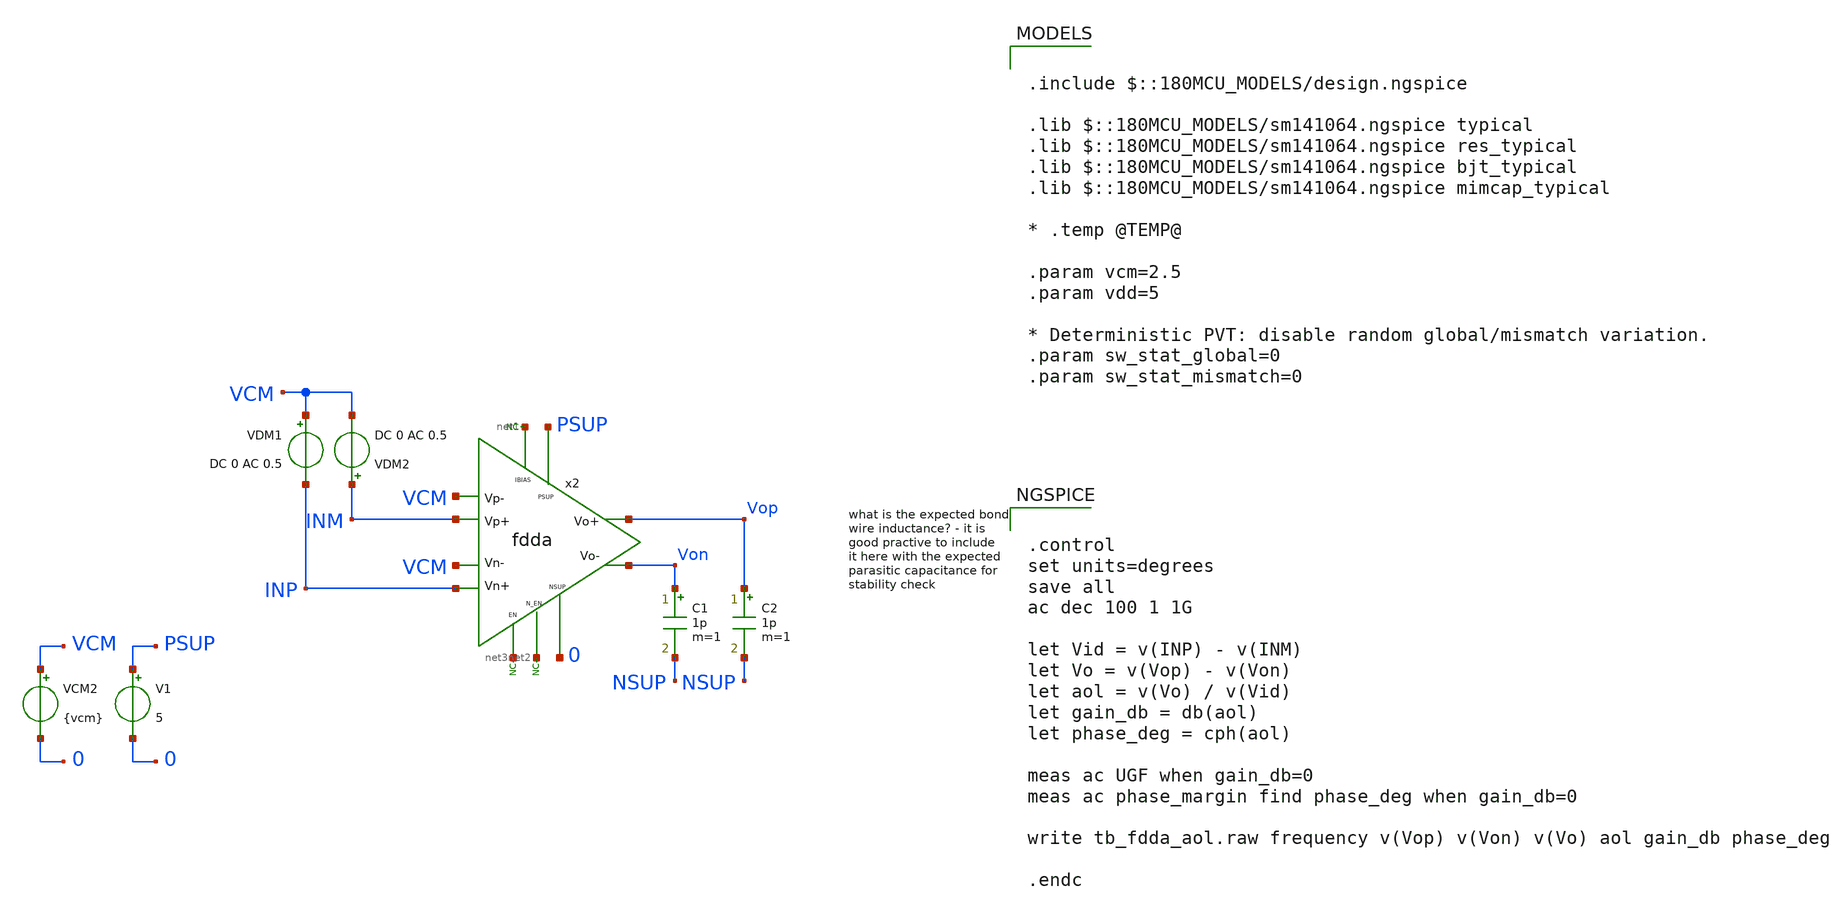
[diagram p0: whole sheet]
** sch_path: xschem/blocks/fdda/tb_fdda_aol.sch
**.subckt tb_fdda_aol
C1 Von NSUP 1p m=1
x2 PSUP VCM VCM INP INM Vop Von net1 net2 net3 0 fdda
* noconn #net1
* noconn #net3
* noconn #net2
V1 PSUP 0 5
C2 Vop NSUP 1p m=1
VCM2 VCM 0 {vcm}
VDM2 INM VCM DC 0 AC 0.5
VDM1 VCM INP DC 0 AC 0.5
**** begin user architecture code

.include $::180MCU_MODELS/design.ngspice

.lib $::180MCU_MODELS/sm141064.ngspice typical
.lib $::180MCU_MODELS/sm141064.ngspice res_typical
.lib $::180MCU_MODELS/sm141064.ngspice bjt_typical
.lib $::180MCU_MODELS/sm141064.ngspice mimcap_typical

* .temp @TEMP@

.param vcm=2.5
.param vdd=5

* Deterministic PVT: disable random global/mismatch variation.
.param sw_stat_global=0
.param sw_stat_mismatch=0



.control
set units=degrees
save all
ac dec 100 1 1G

let Vid = v(INP) - v(INM)
let Vo = v(Vop) - v(Von)
let aol = v(Vo) / v(Vid)
let gain_db = db(aol)
let phase_deg = cph(aol)

meas ac UGF when gain_db=0
meas ac phase_margin find phase_deg when gain_db=0

write tb_fdda_aol.raw frequency v(Vop) v(Von) v(Vo) aol gain_db phase_deg

.endc


**** end user architecture code
**.ends

* expanding   symbol:  blocks/fdda/fdda.sym # of pins=11
** sym_path: xschem/blocks/fdda/fdda.sym
** sch_path: xschem/blocks/fdda/fdda.sch
.subckt fdda PSUP Vp- Vn+ Vn- Vp+ Vo+ Vo- IBIAS N_EN EN NSUP
*.ipin PSUP
*.ipin NSUP
*.ipin N_EN
*.ipin EN
*.ipin IBIAS
*.ipin Vp+
*.ipin Vp-
*.ipin Vn+
*.ipin Vn-
*.opin Vo+
*.opin Vo-
* noconn N_EN
* noconn EN
I0 net5 NSUP 1u
XM9 Vo+ Vp- net1 NSUP pfet_06v0 L=2u W=4u nf=5 ad='int((nf+1)/2) * W/nf * 0.18u' as='int((nf+2)/2) * W/nf * 0.18u'
+ pd='2*int((nf+1)/2) * (W/nf + 0.18u)' ps='2*int((nf+2)/2) * (W/nf + 0.18u)' nrd='0.18u / W' nrs='0.18u / W'
+ sa=0 sb=0 sd=0 m=10
XM1 Vo- Vp+ net1 NSUP pfet_06v0 L=2u W=4u nf=5 ad='int((nf+1)/2) * W/nf * 0.18u' as='int((nf+2)/2) * W/nf * 0.18u'
+ pd='2*int((nf+1)/2) * (W/nf + 0.18u)' ps='2*int((nf+2)/2) * (W/nf + 0.18u)' nrd='0.18u / W' nrs='0.18u / W'
+ sa=0 sb=0 sd=0 m=10
XM2 net1 vb1 PSUP net3 pfet_06v0 L=4u W=2u nf=1 ad='int((nf+1)/2) * W/nf * 0.18u' as='int((nf+2)/2) * W/nf * 0.18u'
+ pd='2*int((nf+1)/2) * (W/nf + 0.18u)' ps='2*int((nf+2)/2) * (W/nf + 0.18u)' nrd='0.18u / W' nrs='0.18u / W'
+ sa=0 sb=0 sd=0 m=8
XM3 Vo- Vo- NSUP NSUP nfet_06v0 L=4u W=2u nf=1 ad='int((nf+1)/2) * W/nf * 0.18u' as='int((nf+2)/2) * W/nf * 0.18u'
+ pd='2*int((nf+1)/2) * (W/nf + 0.18u)' ps='2*int((nf+2)/2) * (W/nf + 0.18u)' nrd='0.18u / W' nrs='0.18u / W'
+ sa=0 sb=0 sd=0 m=4
XM4 Vo+ Vn- net2 NSUP pfet_06v0 L=2u W=4u nf=5 ad='int((nf+1)/2) * W/nf * 0.18u' as='int((nf+2)/2) * W/nf * 0.18u'
+ pd='2*int((nf+1)/2) * (W/nf + 0.18u)' ps='2*int((nf+2)/2) * (W/nf + 0.18u)' nrd='0.18u / W' nrs='0.18u / W'
+ sa=0 sb=0 sd=0 m=10
XM5 Vo- Vn+ net2 NSUP pfet_06v0 L=2u W=4u nf=5 ad='int((nf+1)/2) * W/nf * 0.18u' as='int((nf+2)/2) * W/nf * 0.18u'
+ pd='2*int((nf+1)/2) * (W/nf + 0.18u)' ps='2*int((nf+2)/2) * (W/nf + 0.18u)' nrd='0.18u / W' nrs='0.18u / W'
+ sa=0 sb=0 sd=0 m=10
XM6 net2 vb1 PSUP PSUP pfet_06v0 L=4u W=2u nf=1 ad='int((nf+1)/2) * W/nf * 0.18u' as='int((nf+2)/2) * W/nf * 0.18u'
+ pd='2*int((nf+1)/2) * (W/nf + 0.18u)' ps='2*int((nf+2)/2) * (W/nf + 0.18u)' nrd='0.18u / W' nrs='0.18u / W'
+ sa=0 sb=0 sd=0 m=8
XM8 Vo+ Vo+ NSUP NSUP nfet_06v0 L=4u W=2u nf=1 ad='int((nf+1)/2) * W/nf * 0.18u' as='int((nf+2)/2) * W/nf * 0.18u'
+ pd='2*int((nf+1)/2) * (W/nf + 0.18u)' ps='2*int((nf+2)/2) * (W/nf + 0.18u)' nrd='0.18u / W' nrs='0.18u / W'
+ sa=0 sb=0 sd=0 m=4
XM7 net5 vb1 PSUP net4 pfet_06v0 L=4u W=2u nf=1 ad='int((nf+1)/2) * W/nf * 0.18u' as='int((nf+2)/2) * W/nf * 0.18u'
+ pd='2*int((nf+1)/2) * (W/nf + 0.18u)' ps='2*int((nf+2)/2) * (W/nf + 0.18u)' nrd='0.18u / W' nrs='0.18u / W'
+ sa=0 sb=0 sd=0 m=4
.ends

.end
